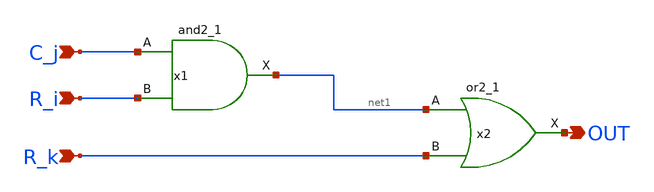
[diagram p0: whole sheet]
** sch_path: DAC/xschem/digital_cell/local_decoder.sch
**.subckt local_decoder C_j R_k R_i OUT
*.ipin C_j
*.ipin R_k
*.ipin R_i
*.opin OUT
x1 C_j R_i VGND VNB VPB VPWR net1 gf180mcu_fd_sc_mcu7t5v0__and2_1
x2 net1 R_k VGND VNB VPB VPWR OUT gf180mcu_fd_sc_mcu7t5v0__or2_1
**.ends
.end
